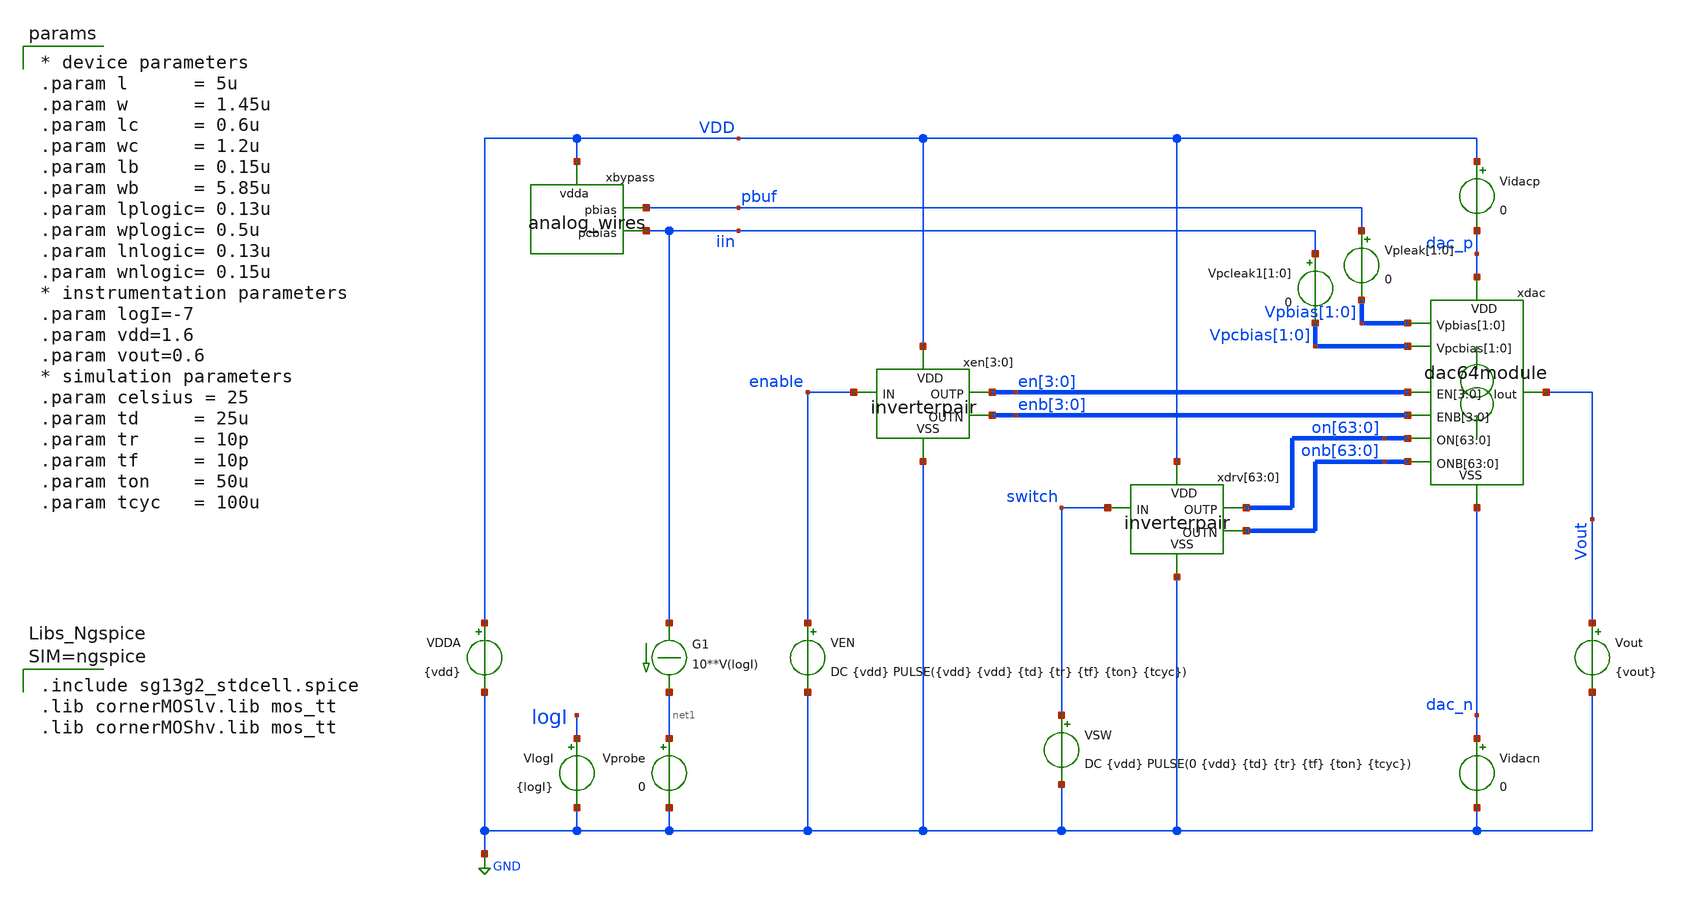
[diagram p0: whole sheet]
** sch_path: xschem/test_dac64_dc.sch
**.subckt test_dac64_dc
Vout Vout GND {vout}
.save i(vout)
Vprobe net1 GND 0
.save i(vprobe)
G1 iin net1 CUR=' 10**V(logI) '
VlogI logI GND {logI}
.save i(vlogi)
VDDA VDD GND {vdd}
.save i(vdda)
VSW switch GND DC {vdd} PULSE(0 {vdd} {td} {tr} {tf} {ton} {tcyc})
.save i(vsw)
Vidacp VDD dac_p 0
.save i(vidacp)
Vidacn dac_n GND 0
.save i(vidacn)
Vpleak[1] pbuf Vpbias[1] 0
Vpleak[0] pbuf Vpbias[0] 0
.save i(vpleak[1])
.save i(vpleak[0])
xdac dac_p en[3] en[2] en[1] en[0] enb[3] enb[2] enb[1] enb[0] on[63] on[62] on[61] on[60] on[59]
+ on[58] on[57] on[56] on[55] on[54] on[53] on[52] on[51] on[50] on[49] on[48] on[47] on[46] on[45] on[44]
+ on[43] on[42] on[41] on[40] on[39] on[38] on[37] on[36] on[35] on[34] on[33] on[32] on[31] on[30] on[29]
+ on[28] on[27] on[26] on[25] on[24] on[23] on[22] on[21] on[20] on[19] on[18] on[17] on[16] on[15] on[14]
+ on[13] on[12] on[11] on[10] on[9] on[8] on[7] on[6] on[5] on[4] on[3] on[2] on[1] on[0] onb[63] onb[62]
+ onb[61] onb[60] onb[59] onb[58] onb[57] onb[56] onb[55] onb[54] onb[53] onb[52] onb[51] onb[50] onb[49]
+ onb[48] onb[47] onb[46] onb[45] onb[44] onb[43] onb[42] onb[41] onb[40] onb[39] onb[38] onb[37] onb[36]
+ onb[35] onb[34] onb[33] onb[32] onb[31] onb[30] onb[29] onb[28] onb[27] onb[26] onb[25] onb[24] onb[23]
+ onb[22] onb[21] onb[20] onb[19] onb[18] onb[17] onb[16] onb[15] onb[14] onb[13] onb[12] onb[11] onb[10]
+ onb[9] onb[8] onb[7] onb[6] onb[5] onb[4] onb[3] onb[2] onb[1] onb[0] Vout Vpbias[1] Vpbias[0] Vpcbias[1]
+ Vpcbias[0] dac_n dac64module
xbypass VDD pbuf iin analog_wires
Vpcleak1[1] iin Vpcbias[1] 0
Vpcleak1[0] iin Vpcbias[0] 0
.save i(vpcleak1[1])
.save i(vpcleak1[0])
xen[3] VDD en[3] enable enb[3] GND inverterpair
xen[2] VDD en[2] enable enb[2] GND inverterpair
xen[1] VDD en[1] enable enb[1] GND inverterpair
xen[0] VDD en[0] enable enb[0] GND inverterpair
xdrv[63] VDD on[63] switch onb[63] GND inverterpair
xdrv[62] VDD on[62] switch onb[62] GND inverterpair
xdrv[61] VDD on[61] switch onb[61] GND inverterpair
xdrv[60] VDD on[60] switch onb[60] GND inverterpair
xdrv[59] VDD on[59] switch onb[59] GND inverterpair
xdrv[58] VDD on[58] switch onb[58] GND inverterpair
xdrv[57] VDD on[57] switch onb[57] GND inverterpair
xdrv[56] VDD on[56] switch onb[56] GND inverterpair
xdrv[55] VDD on[55] switch onb[55] GND inverterpair
xdrv[54] VDD on[54] switch onb[54] GND inverterpair
xdrv[53] VDD on[53] switch onb[53] GND inverterpair
xdrv[52] VDD on[52] switch onb[52] GND inverterpair
xdrv[51] VDD on[51] switch onb[51] GND inverterpair
xdrv[50] VDD on[50] switch onb[50] GND inverterpair
xdrv[49] VDD on[49] switch onb[49] GND inverterpair
xdrv[48] VDD on[48] switch onb[48] GND inverterpair
xdrv[47] VDD on[47] switch onb[47] GND inverterpair
xdrv[46] VDD on[46] switch onb[46] GND inverterpair
xdrv[45] VDD on[45] switch onb[45] GND inverterpair
xdrv[44] VDD on[44] switch onb[44] GND inverterpair
xdrv[43] VDD on[43] switch onb[43] GND inverterpair
xdrv[42] VDD on[42] switch onb[42] GND inverterpair
xdrv[41] VDD on[41] switch onb[41] GND inverterpair
xdrv[40] VDD on[40] switch onb[40] GND inverterpair
xdrv[39] VDD on[39] switch onb[39] GND inverterpair
xdrv[38] VDD on[38] switch onb[38] GND inverterpair
xdrv[37] VDD on[37] switch onb[37] GND inverterpair
xdrv[36] VDD on[36] switch onb[36] GND inverterpair
xdrv[35] VDD on[35] switch onb[35] GND inverterpair
xdrv[34] VDD on[34] switch onb[34] GND inverterpair
xdrv[33] VDD on[33] switch onb[33] GND inverterpair
xdrv[32] VDD on[32] switch onb[32] GND inverterpair
xdrv[31] VDD on[31] switch onb[31] GND inverterpair
xdrv[30] VDD on[30] switch onb[30] GND inverterpair
xdrv[29] VDD on[29] switch onb[29] GND inverterpair
xdrv[28] VDD on[28] switch onb[28] GND inverterpair
xdrv[27] VDD on[27] switch onb[27] GND inverterpair
xdrv[26] VDD on[26] switch onb[26] GND inverterpair
xdrv[25] VDD on[25] switch onb[25] GND inverterpair
xdrv[24] VDD on[24] switch onb[24] GND inverterpair
xdrv[23] VDD on[23] switch onb[23] GND inverterpair
xdrv[22] VDD on[22] switch onb[22] GND inverterpair
xdrv[21] VDD on[21] switch onb[21] GND inverterpair
xdrv[20] VDD on[20] switch onb[20] GND inverterpair
xdrv[19] VDD on[19] switch onb[19] GND inverterpair
xdrv[18] VDD on[18] switch onb[18] GND inverterpair
xdrv[17] VDD on[17] switch onb[17] GND inverterpair
xdrv[16] VDD on[16] switch onb[16] GND inverterpair
xdrv[15] VDD on[15] switch onb[15] GND inverterpair
xdrv[14] VDD on[14] switch onb[14] GND inverterpair
xdrv[13] VDD on[13] switch onb[13] GND inverterpair
xdrv[12] VDD on[12] switch onb[12] GND inverterpair
xdrv[11] VDD on[11] switch onb[11] GND inverterpair
xdrv[10] VDD on[10] switch onb[10] GND inverterpair
xdrv[9] VDD on[9] switch onb[9] GND inverterpair
xdrv[8] VDD on[8] switch onb[8] GND inverterpair
xdrv[7] VDD on[7] switch onb[7] GND inverterpair
xdrv[6] VDD on[6] switch onb[6] GND inverterpair
xdrv[5] VDD on[5] switch onb[5] GND inverterpair
xdrv[4] VDD on[4] switch onb[4] GND inverterpair
xdrv[3] VDD on[3] switch onb[3] GND inverterpair
xdrv[2] VDD on[2] switch onb[2] GND inverterpair
xdrv[1] VDD on[1] switch onb[1] GND inverterpair
xdrv[0] VDD on[0] switch onb[0] GND inverterpair
VEN enable GND DC {vdd} PULSE({vdd} {vdd} {td} {tr} {tf} {ton} {tcyc})
.save i(ven)
**** begin user architecture code


.include test_dac64_dc.save
.temp=27
.options gmin=1e-15 abstol=1p method=gear
.options savecurrents
.control
save all
op
write test_dac64_dc.raw
set appendwrite
dc Vout 0 1.6 10m VlogI -8 -6 0.5
*tran 10n 500u
write test_dac64_dc.raw
plot title "output/reference current asymmetry"
+ 2*(vout#branch-16*vprobe#branch)/(16*vprobe#branch+vout#branch)
plot ylimit -20m 4m title "output/reference current asymmetry"
+ 2*(vout#branch-16*vprobe#branch)/(16*vprobe#branch+vout#branch)
plot vdd pbuf iin enable switch v("en[0]") v("enb[0]") v("on[0]") v("onb[0]") Vout
plot vout#branch vprobe#branch
*plot @n.xsw.xmbias.nsg13_lv_pmos[ids] @n.xsw.xmpullup.nsg13_lv_pmos[ids]
plot vidacp#branch vidacn#branch
*plot 0.5*(vidacp#branch+vidacn#branch) vidacp#branch-vidacn#branch
.endc




.include sg13g2_stdcell.spice
.lib cornerMOSlv.lib mos_tt
.lib cornerMOShv.lib mos_tt



* device parameters
.param l      = 5u
.param w      = 1.45u
.param lc     = 0.6u
.param wc     = 1.2u
.param lb     = 0.15u
.param wb     = 5.85u
.param lplogic= 0.13u
.param wplogic= 0.5u
.param lnlogic= 0.13u
.param wnlogic= 0.15u
* instrumentation parameters
.param logI=-7
.param vdd=1.6
.param vout=0.6
* simulation parameters
.param celsius = 25
.param td     = 25u
.param tr     = 10p
.param tf     = 10p
.param ton    = 50u
.param tcyc   = 100u


**** end user architecture code
**.ends

* expanding   symbol:  dac64module.sym # of pins=9
** sym_path: xschem/dac64module.sym
** sch_path: xschem/dac64module.sch
.subckt dac64module VDD EN[3] EN[2] EN[1] EN[0] ENB[3] ENB[2] ENB[1] ENB[0] ON[63] ON[62] ON[61]
+ ON[60] ON[59] ON[58] ON[57] ON[56] ON[55] ON[54] ON[53] ON[52] ON[51] ON[50] ON[49] ON[48] ON[47] ON[46]
+ ON[45] ON[44] ON[43] ON[42] ON[41] ON[40] ON[39] ON[38] ON[37] ON[36] ON[35] ON[34] ON[33] ON[32] ON[31]
+ ON[30] ON[29] ON[28] ON[27] ON[26] ON[25] ON[24] ON[23] ON[22] ON[21] ON[20] ON[19] ON[18] ON[17] ON[16]
+ ON[15] ON[14] ON[13] ON[12] ON[11] ON[10] ON[9] ON[8] ON[7] ON[6] ON[5] ON[4] ON[3] ON[2] ON[1] ON[0]
+ ONB[63] ONB[62] ONB[61] ONB[60] ONB[59] ONB[58] ONB[57] ONB[56] ONB[55] ONB[54] ONB[53] ONB[52] ONB[51]
+ ONB[50] ONB[49] ONB[48] ONB[47] ONB[46] ONB[45] ONB[44] ONB[43] ONB[42] ONB[41] ONB[40] ONB[39] ONB[38]
+ ONB[37] ONB[36] ONB[35] ONB[34] ONB[33] ONB[32] ONB[31] ONB[30] ONB[29] ONB[28] ONB[27] ONB[26] ONB[25]
+ ONB[24] ONB[23] ONB[22] ONB[21] ONB[20] ONB[19] ONB[18] ONB[17] ONB[16] ONB[15] ONB[14] ONB[13] ONB[12]
+ ONB[11] ONB[10] ONB[9] ONB[8] ONB[7] ONB[6] ONB[5] ONB[4] ONB[3] ONB[2] ONB[1] ONB[0] Iout Vpbias[1]
+ Vpbias[0] Vpcbias[1] Vpcbias[0] VSS
*.opin Iout
*.ipin
*+ ON[63],ON[62],ON[61],ON[60],ON[59],ON[58],ON[57],ON[56],ON[55],ON[54],ON[53],ON[52],ON[51],ON[50],ON[49],ON[48],ON[47],ON[46],ON[45],ON[44],ON[43],ON[42],ON[41],ON[40],ON[39],ON[38],ON[37],ON[36],ON[35],ON[34],ON[33],ON[32],ON[31],ON[30],ON[29],ON[28],ON[27],ON[26],ON[25],ON[24],ON[23],ON[22],ON[21],ON[20],ON[19],ON[18],ON[17],ON[16],ON[15],ON[14],ON[13],ON[12],ON[11],ON[10],ON[9],ON[8],ON[7],ON[6],ON[5],ON[4],ON[3],ON[2],ON[1],ON[0]
*.ipin
*+ ONB[63],ONB[62],ONB[61],ONB[60],ONB[59],ONB[58],ONB[57],ONB[56],ONB[55],ONB[54],ONB[53],ONB[52],ONB[51],ONB[50],ONB[49],ONB[48],ONB[47],ONB[46],ONB[45],ONB[44],ONB[43],ONB[42],ONB[41],ONB[40],ONB[39],ONB[38],ONB[37],ONB[36],ONB[35],ONB[34],ONB[33],ONB[32],ONB[31],ONB[30],ONB[29],ONB[28],ONB[27],ONB[26],ONB[25],ONB[24],ONB[23],ONB[22],ONB[21],ONB[20],ONB[19],ONB[18],ONB[17],ONB[16],ONB[15],ONB[14],ONB[13],ONB[12],ONB[11],ONB[10],ONB[9],ONB[8],ONB[7],ONB[6],ONB[5],ONB[4],ONB[3],ONB[2],ONB[1],ONB[0]
*.iopin VSS
*.iopin VDD
*.iopin Vpcbias[1],Vpcbias[0]
*.ipin EN[3],EN[2],EN[1],EN[0]
*.ipin ENB[3],ENB[2],ENB[1],ENB[0]
*.iopin Vpbias[1],Vpbias[0]
XMcbias[0] Vpcbias[0] Vpcbias[0] Vpbias[0] VDD sg13_lv_pmos w=5.85u l=0.15u ng=1 m=2 mm_ok=1
**** begin user architecture code

* device parameters
.param l      = 5u
.param w      = 1.45u
.param lc     = 0.6u
.param wc     = 1.2u
.param lb     = 0.15u
.param wb     = 5.85u
.param lplogic= 0.13u
.param wplogic= 0.5u
.param lnlogic= 0.13u
.param wnlogic= 0.15u


**** end user architecture code
xref[1] VDD Vpbias[0] EN[1] ENB[1] Vpbias[0] Vpcbias[0] VSS unitsource2u
xref[0] VDD Vpbias[0] EN[0] ENB[0] Vpbias[0] Vpcbias[0] VSS unitsource2u
xsrc[31] VDD Vpbias[0] ON[31] ONB[31] Iout Vpcbias[0] VSS unitsource2u
xsrc[30] VDD Vpbias[0] ON[30] ONB[30] Iout Vpcbias[0] VSS unitsource2u
xsrc[29] VDD Vpbias[0] ON[29] ONB[29] Iout Vpcbias[0] VSS unitsource2u
xsrc[28] VDD Vpbias[0] ON[28] ONB[28] Iout Vpcbias[0] VSS unitsource2u
xsrc[27] VDD Vpbias[0] ON[27] ONB[27] Iout Vpcbias[0] VSS unitsource2u
xsrc[26] VDD Vpbias[0] ON[26] ONB[26] Iout Vpcbias[0] VSS unitsource2u
xsrc[25] VDD Vpbias[0] ON[25] ONB[25] Iout Vpcbias[0] VSS unitsource2u
xsrc[24] VDD Vpbias[0] ON[24] ONB[24] Iout Vpcbias[0] VSS unitsource2u
xsrc[23] VDD Vpbias[0] ON[23] ONB[23] Iout Vpcbias[0] VSS unitsource2u
xsrc[22] VDD Vpbias[0] ON[22] ONB[22] Iout Vpcbias[0] VSS unitsource2u
xsrc[21] VDD Vpbias[0] ON[21] ONB[21] Iout Vpcbias[0] VSS unitsource2u
xsrc[20] VDD Vpbias[0] ON[20] ONB[20] Iout Vpcbias[0] VSS unitsource2u
xsrc[19] VDD Vpbias[0] ON[19] ONB[19] Iout Vpcbias[0] VSS unitsource2u
xsrc[18] VDD Vpbias[0] ON[18] ONB[18] Iout Vpcbias[0] VSS unitsource2u
xsrc[17] VDD Vpbias[0] ON[17] ONB[17] Iout Vpcbias[0] VSS unitsource2u
xsrc[16] VDD Vpbias[0] ON[16] ONB[16] Iout Vpcbias[0] VSS unitsource2u
xsrc[15] VDD Vpbias[0] ON[15] ONB[15] Iout Vpcbias[0] VSS unitsource2u
xsrc[14] VDD Vpbias[0] ON[14] ONB[14] Iout Vpcbias[0] VSS unitsource2u
xsrc[13] VDD Vpbias[0] ON[13] ONB[13] Iout Vpcbias[0] VSS unitsource2u
xsrc[12] VDD Vpbias[0] ON[12] ONB[12] Iout Vpcbias[0] VSS unitsource2u
xsrc[11] VDD Vpbias[0] ON[11] ONB[11] Iout Vpcbias[0] VSS unitsource2u
xsrc[10] VDD Vpbias[0] ON[10] ONB[10] Iout Vpcbias[0] VSS unitsource2u
xsrc[9] VDD Vpbias[0] ON[9] ONB[9] Iout Vpcbias[0] VSS unitsource2u
xsrc[8] VDD Vpbias[0] ON[8] ONB[8] Iout Vpcbias[0] VSS unitsource2u
xsrc[7] VDD Vpbias[0] ON[7] ONB[7] Iout Vpcbias[0] VSS unitsource2u
xsrc[6] VDD Vpbias[0] ON[6] ONB[6] Iout Vpcbias[0] VSS unitsource2u
xsrc[5] VDD Vpbias[0] ON[5] ONB[5] Iout Vpcbias[0] VSS unitsource2u
xsrc[4] VDD Vpbias[0] ON[4] ONB[4] Iout Vpcbias[0] VSS unitsource2u
xsrc[3] VDD Vpbias[0] ON[3] ONB[3] Iout Vpcbias[0] VSS unitsource2u
xsrc[2] VDD Vpbias[0] ON[2] ONB[2] Iout Vpcbias[0] VSS unitsource2u
xsrc[1] VDD Vpbias[0] ON[1] ONB[1] Iout Vpcbias[0] VSS unitsource2u
xsrc[0] VDD Vpbias[0] ON[0] ONB[0] Iout Vpcbias[0] VSS unitsource2u
XMcbias[1] Vpcbias[1] Vpcbias[1] Vpbias[1] VDD sg13_lv_pmos w=5.85u l=0.15u ng=1 m=2 mm_ok=1
xref1[3] VDD Vpbias[1] EN[3] ENB[3] Vpbias[1] Vpcbias[1] VSS unitsource2u
xref1[2] VDD Vpbias[1] EN[2] ENB[2] Vpbias[1] Vpcbias[1] VSS unitsource2u
xsrc1[63] VDD Vpbias[1] ON[63] ONB[63] Iout Vpcbias[1] VSS unitsource2u
xsrc1[62] VDD Vpbias[1] ON[62] ONB[62] Iout Vpcbias[1] VSS unitsource2u
xsrc1[61] VDD Vpbias[1] ON[61] ONB[61] Iout Vpcbias[1] VSS unitsource2u
xsrc1[60] VDD Vpbias[1] ON[60] ONB[60] Iout Vpcbias[1] VSS unitsource2u
xsrc1[59] VDD Vpbias[1] ON[59] ONB[59] Iout Vpcbias[1] VSS unitsource2u
xsrc1[58] VDD Vpbias[1] ON[58] ONB[58] Iout Vpcbias[1] VSS unitsource2u
xsrc1[57] VDD Vpbias[1] ON[57] ONB[57] Iout Vpcbias[1] VSS unitsource2u
xsrc1[56] VDD Vpbias[1] ON[56] ONB[56] Iout Vpcbias[1] VSS unitsource2u
xsrc1[55] VDD Vpbias[1] ON[55] ONB[55] Iout Vpcbias[1] VSS unitsource2u
xsrc1[54] VDD Vpbias[1] ON[54] ONB[54] Iout Vpcbias[1] VSS unitsource2u
xsrc1[53] VDD Vpbias[1] ON[53] ONB[53] Iout Vpcbias[1] VSS unitsource2u
xsrc1[52] VDD Vpbias[1] ON[52] ONB[52] Iout Vpcbias[1] VSS unitsource2u
xsrc1[51] VDD Vpbias[1] ON[51] ONB[51] Iout Vpcbias[1] VSS unitsource2u
xsrc1[50] VDD Vpbias[1] ON[50] ONB[50] Iout Vpcbias[1] VSS unitsource2u
xsrc1[49] VDD Vpbias[1] ON[49] ONB[49] Iout Vpcbias[1] VSS unitsource2u
xsrc1[48] VDD Vpbias[1] ON[48] ONB[48] Iout Vpcbias[1] VSS unitsource2u
xsrc1[47] VDD Vpbias[1] ON[47] ONB[47] Iout Vpcbias[1] VSS unitsource2u
xsrc1[46] VDD Vpbias[1] ON[46] ONB[46] Iout Vpcbias[1] VSS unitsource2u
xsrc1[45] VDD Vpbias[1] ON[45] ONB[45] Iout Vpcbias[1] VSS unitsource2u
xsrc1[44] VDD Vpbias[1] ON[44] ONB[44] Iout Vpcbias[1] VSS unitsource2u
xsrc1[43] VDD Vpbias[1] ON[43] ONB[43] Iout Vpcbias[1] VSS unitsource2u
xsrc1[42] VDD Vpbias[1] ON[42] ONB[42] Iout Vpcbias[1] VSS unitsource2u
xsrc1[41] VDD Vpbias[1] ON[41] ONB[41] Iout Vpcbias[1] VSS unitsource2u
xsrc1[40] VDD Vpbias[1] ON[40] ONB[40] Iout Vpcbias[1] VSS unitsource2u
xsrc1[39] VDD Vpbias[1] ON[39] ONB[39] Iout Vpcbias[1] VSS unitsource2u
xsrc1[38] VDD Vpbias[1] ON[38] ONB[38] Iout Vpcbias[1] VSS unitsource2u
xsrc1[37] VDD Vpbias[1] ON[37] ONB[37] Iout Vpcbias[1] VSS unitsource2u
xsrc1[36] VDD Vpbias[1] ON[36] ONB[36] Iout Vpcbias[1] VSS unitsource2u
xsrc1[35] VDD Vpbias[1] ON[35] ONB[35] Iout Vpcbias[1] VSS unitsource2u
xsrc1[34] VDD Vpbias[1] ON[34] ONB[34] Iout Vpcbias[1] VSS unitsource2u
xsrc1[33] VDD Vpbias[1] ON[33] ONB[33] Iout Vpcbias[1] VSS unitsource2u
xsrc1[32] VDD Vpbias[1] ON[32] ONB[32] Iout Vpcbias[1] VSS unitsource2u
* tap: EN[3:0] --> EN[1:0]
* tap: ENB[3:0] --> ENB[1:0]
* tap: ENB[3:0] --> ENB[3:2]
* tap: EN[3:0] --> EN[3:2]
* tap: ON[63:0] --> ON[31:0]
* tap: ONB[63:0] --> ONB[31:0]
* tap: ON[63:0] --> ON[63:32]
* tap: ONB[63:0] --> ONB[63:32]
* tap: Vpbias[1:0] --> Vpbias[0]
* tap: Vpcbias[1:0] --> Vpcbias[0]
* tap: Vpbias[1:0] --> Vpbias[1]
* tap: Vpcbias[1:0] --> Vpcbias[1]
.ends


* expanding   symbol:  analog_wires.sym # of pins=3
** sym_path: xschem/analog_wires.sym
** sch_path: xschem/analog_wires.sch
.subckt analog_wires vdda pbias pcbias
*.iopin vdda
*.iopin pcbias
*.iopin pbias
XMcbuffer vdda pcbias vdda vdda sg13_hv_pmos w=8u l=8u ng=1 m=19 mm_ok=1
XMbbuffer vdda pbias vdda vdda sg13_hv_pmos w=8u l=8u ng=1 m=19 mm_ok=1
.ends


* expanding   symbol:  inverterpair.sym # of pins=5
** sym_path: xschem/inverterpair.sym
** sch_path: xschem/inverterpair.sch
.subckt inverterpair VDD OUTP IN OUTN VSS
*.iopin VSS
*.ipin IN
*.opin OUTN
*.opin OUTP
*.iopin VDD
xinv2 OUTP OUTN VDD VSS sg13g2_inv_1
xinv1 OUTN IN VDD VSS sg13g2_inv_1
.ends


* expanding   symbol:  unitsource2u.sym # of pins=7
** sym_path: xschem/unitsource2u.sym
** sch_path: xschem/unitsource2u.sch
.subckt unitsource2u VDD VbiasP ON ONB Iout VcascP VSS
*.iopin VSS
*.iopin VDD
*.iopin VbiasP
*.iopin VcascP
*.ipin ON
*.ipin ONB
*.iopin Iout
xnonoverlap VDD VSS ON ONB on_n off_n nonoverlap
xsw VDD off_n Vcasc on_n VcascP cascodeswitch_pmos
xsrc VDD VbiasP Vcasc Iout pcsource2u
.ends


* expanding   symbol:  sg13g2_stdcells/sg13g2_inv_1.sym # of pins=2
** sym_path: sg13g2_stdcells/sg13g2_inv_1.sym
** sch_path: sg13g2_stdcells/sg13g2_inv_1.sch
.subckt sg13g2_inv_1 Y A VDD VSS
*.opin Y
*.ipin A
*.iopin VDD
*.iopin VSS
XM1 Y A VSS VSS sg13_lv_nmos w=740.00n l=130.00n ng=1 m=1 mm_ok=1
XM2 Y A VDD VDD sg13_lv_pmos w=1.12u l=130.00n ng=1 m=1 mm_ok=1
.ends


* expanding   symbol:  nonoverlap.sym # of pins=6
** sym_path: xschem/nonoverlap.sym
** sch_path: xschem/nonoverlap.sch
.subckt nonoverlap VDD VSS INP INN OUTN OUTP
*.iopin VSS
*.iopin VDD
*.ipin INP
*.ipin INN
*.opin OUTP
*.opin OUTN
XM1 OUTN INP VDD VDD sg13_lv_pmos w=0.3u l=0.13u ng=1 m=1 mm_ok=1
XM2 OUTP INN VDD VDD sg13_lv_pmos w=0.3u l=0.13u ng=1 m=1 mm_ok=1
XM3 OUTN OUTP VSS VSS sg13_lv_nmos w=0.15u l=0.52u ng=1 m=1 mm_ok=1
XM4 OUTP OUTN VSS VSS sg13_lv_nmos w=0.15u l=0.52u ng=1 m=1 mm_ok=1
.ends


* expanding   symbol:  cascodeswitch_pmos.sym # of pins=5
** sym_path: xschem/cascodeswitch_pmos.sym
** sch_path: xschem/cascodeswitch_pmos.sch
.subckt cascodeswitch_pmos VDD off_n Vcasc on_n Vbpcasc
*.ipin off_n
*.ipin Vbpcasc
*.opin Vcasc
*.ipin on_n
*.ipin VDD
XMpullup Vcasc off_n VDD VDD sg13_lv_pmos w=0.3u l=0.13u ng=1 m=1 mm_ok=1
XMbias Vbpcasc on_n Vcasc VDD sg13_lv_pmos w=0.3u l=0.13u ng=1 m=1 mm_ok=1
.ends


* expanding   symbol:  pcsource2u.sym # of pins=4
** sym_path: xschem/pcsource2u.sym
** sch_path: xschem/pcsource2u.sch
.subckt pcsource2u VDD VbiasP VcascodeP Iout
*.ipin VcascodeP
*.ipin VbiasP
*.opin Iout
*.ipin VDD
XMsrc drain net4 VDD net1 sg13_lv_pmos w=1.45u l=5u ng=1 m=1 mm_ok=1
XMcasc Iout net3 drain net2 sg13_lv_pmos w=1.2u l=0.6u ng=1 m=1 mm_ok=1
Vgsrc net4 VbiasP 0
.save i(vgsrc)
Vgcasc net3 VcascodeP 0
.save i(vgcasc)
Vbsrc VDD net1 0
.save i(vbsrc)
Vbcasc VDD net2 0
.save i(vbcasc)
.ends

.GLOBAL GND
.end
